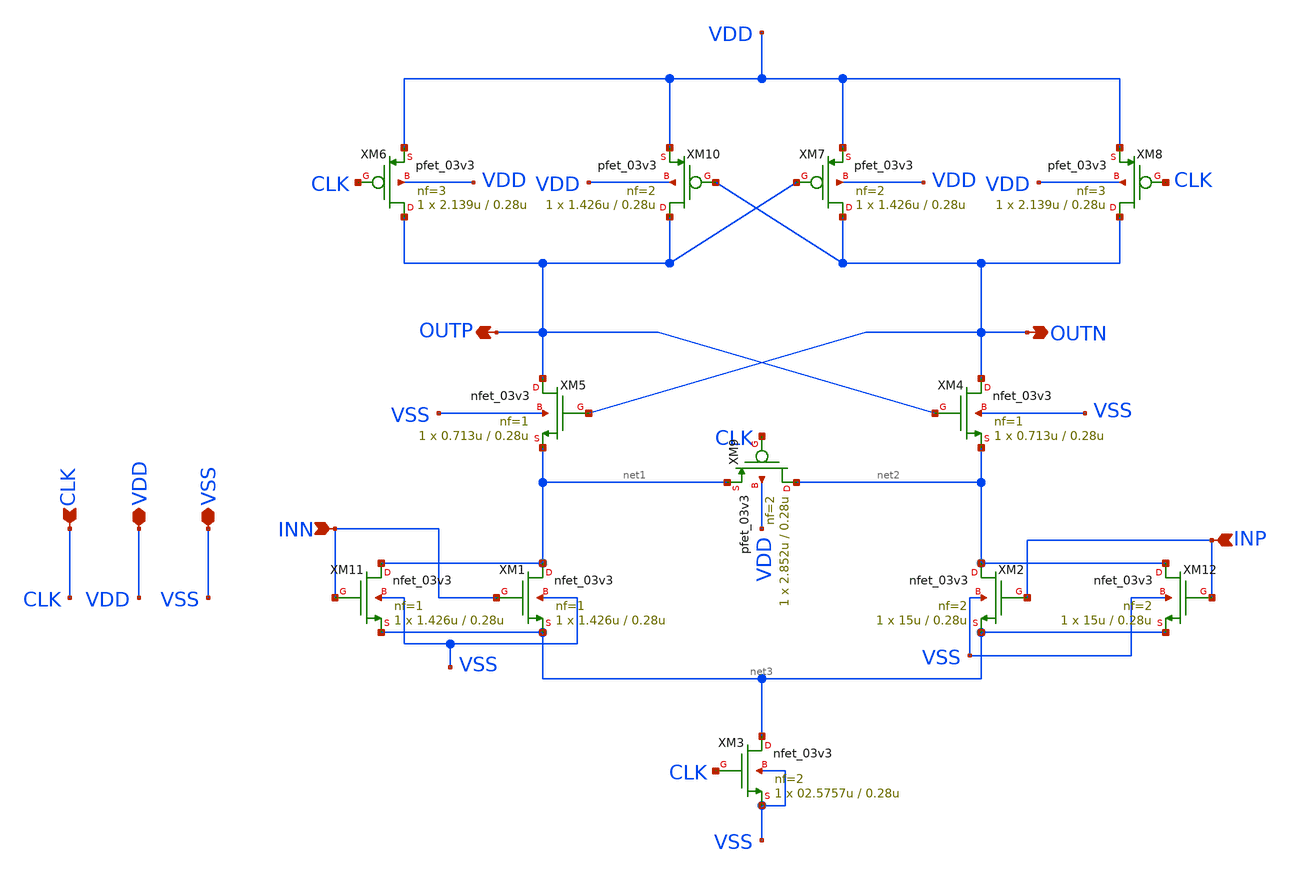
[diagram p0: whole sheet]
** sch_path: analog/blocks/Double_Tail_Comparator/realcomp.sch
**.subckt realcomp CLK VSS VDD OUTP OUTN INN INP
*.ipin CLK
*.iopin VSS
*.iopin VDD
*.opin OUTP
*.opin OUTN
*.ipin INN
*.ipin INP
XM1 net1 INN net3 VSS nfet_03v3 L=0.28u W=1.426u nf=1 ad='int((nf+1)/2) * W/nf * 0.18u' as='int((nf+2)/2) * W/nf * 0.18u'
+ pd='2*int((nf+1)/2) * (W/nf + 0.18u)' ps='2*int((nf+2)/2) * (W/nf + 0.18u)' nrd='0.18u / W' nrs='0.18u / W'
+ sa=0 sb=0 sd=0 m=1
XM2 net2 INP net3 VSS nfet_03v3 L=0.28u W=15u nf=2 ad='int((nf+1)/2) * W/nf * 0.18u' as='int((nf+2)/2) * W/nf * 0.18u'
+ pd='2*int((nf+1)/2) * (W/nf + 0.18u)' ps='2*int((nf+2)/2) * (W/nf + 0.18u)' nrd='0.18u / W' nrs='0.18u / W'
+ sa=0 sb=0 sd=0 m=1
XM3 net3 CLK VSS VSS nfet_03v3 L=0.28u W=02.5757u nf=2 ad='int((nf+1)/2) * W/nf * 0.18u' as='int((nf+2)/2) * W/nf * 0.18u'
+ pd='2*int((nf+1)/2) * (W/nf + 0.18u)' ps='2*int((nf+2)/2) * (W/nf + 0.18u)' nrd='0.18u / W' nrs='0.18u / W'
+ sa=0 sb=0 sd=0 m=1
XM4 OUTN OUTP net2 VSS nfet_03v3 L=0.28u W=0.713u nf=1 ad='int((nf+1)/2) * W/nf * 0.18u' as='int((nf+2)/2) * W/nf * 0.18u'
+ pd='2*int((nf+1)/2) * (W/nf + 0.18u)' ps='2*int((nf+2)/2) * (W/nf + 0.18u)' nrd='0.18u / W' nrs='0.18u / W'
+ sa=0 sb=0 sd=0 m=1
XM5 OUTP OUTN net1 VSS nfet_03v3 L=0.28u W=0.713u nf=1 ad='int((nf+1)/2) * W/nf * 0.18u' as='int((nf+2)/2) * W/nf * 0.18u'
+ pd='2*int((nf+1)/2) * (W/nf + 0.18u)' ps='2*int((nf+2)/2) * (W/nf + 0.18u)' nrd='0.18u / W' nrs='0.18u / W'
+ sa=0 sb=0 sd=0 m=1
XM6 OUTP CLK VDD VDD pfet_03v3 L=0.28u W=2.139u nf=3 ad='int((nf+1)/2) * W/nf * 0.18u' as='int((nf+2)/2) * W/nf * 0.18u'
+ pd='2*int((nf+1)/2) * (W/nf + 0.18u)' ps='2*int((nf+2)/2) * (W/nf + 0.18u)' nrd='0.18u / W' nrs='0.18u / W'
+ sa=0 sb=0 sd=0 m=1
XM7 OUTN OUTP VDD VDD pfet_03v3 L=0.28u W=1.426u nf=2 ad='int((nf+1)/2) * W/nf * 0.18u' as='int((nf+2)/2) * W/nf * 0.18u'
+ pd='2*int((nf+1)/2) * (W/nf + 0.18u)' ps='2*int((nf+2)/2) * (W/nf + 0.18u)' nrd='0.18u / W' nrs='0.18u / W'
+ sa=0 sb=0 sd=0 m=1
XM8 OUTN CLK VDD VDD pfet_03v3 L=0.28u W=2.139u nf=3 ad='int((nf+1)/2) * W/nf * 0.18u' as='int((nf+2)/2) * W/nf * 0.18u'
+ pd='2*int((nf+1)/2) * (W/nf + 0.18u)' ps='2*int((nf+2)/2) * (W/nf + 0.18u)' nrd='0.18u / W' nrs='0.18u / W'
+ sa=0 sb=0 sd=0 m=1
XM10 OUTP OUTN VDD VDD pfet_03v3 L=0.28u W=1.426u nf=2 ad='int((nf+1)/2) * W/nf * 0.18u' as='int((nf+2)/2) * W/nf * 0.18u'
+ pd='2*int((nf+1)/2) * (W/nf + 0.18u)' ps='2*int((nf+2)/2) * (W/nf + 0.18u)' nrd='0.18u / W' nrs='0.18u / W'
+ sa=0 sb=0 sd=0 m=1
XM9 net2 CLK net1 VDD pfet_03v3 L=0.28u W=2.852u nf=2 ad='int((nf+1)/2) * W/nf * 0.18u' as='int((nf+2)/2) * W/nf * 0.18u'
+ pd='2*int((nf+1)/2) * (W/nf + 0.18u)' ps='2*int((nf+2)/2) * (W/nf + 0.18u)' nrd='0.18u / W' nrs='0.18u / W'
+ sa=0 sb=0 sd=0 m=1
XM11 net1 INN net3 VSS nfet_03v3 L=0.28u W=1.426u nf=1 ad='int((nf+1)/2) * W/nf * 0.18u' as='int((nf+2)/2) * W/nf * 0.18u'
+ pd='2*int((nf+1)/2) * (W/nf + 0.18u)' ps='2*int((nf+2)/2) * (W/nf + 0.18u)' nrd='0.18u / W' nrs='0.18u / W'
+ sa=0 sb=0 sd=0 m=1
XM12 net2 INP net3 VSS nfet_03v3 L=0.28u W=15u nf=2 ad='int((nf+1)/2) * W/nf * 0.18u' as='int((nf+2)/2) * W/nf * 0.18u'
+ pd='2*int((nf+1)/2) * (W/nf + 0.18u)' ps='2*int((nf+2)/2) * (W/nf + 0.18u)' nrd='0.18u / W' nrs='0.18u / W'
+ sa=0 sb=0 sd=0 m=1
**.ends
.end
